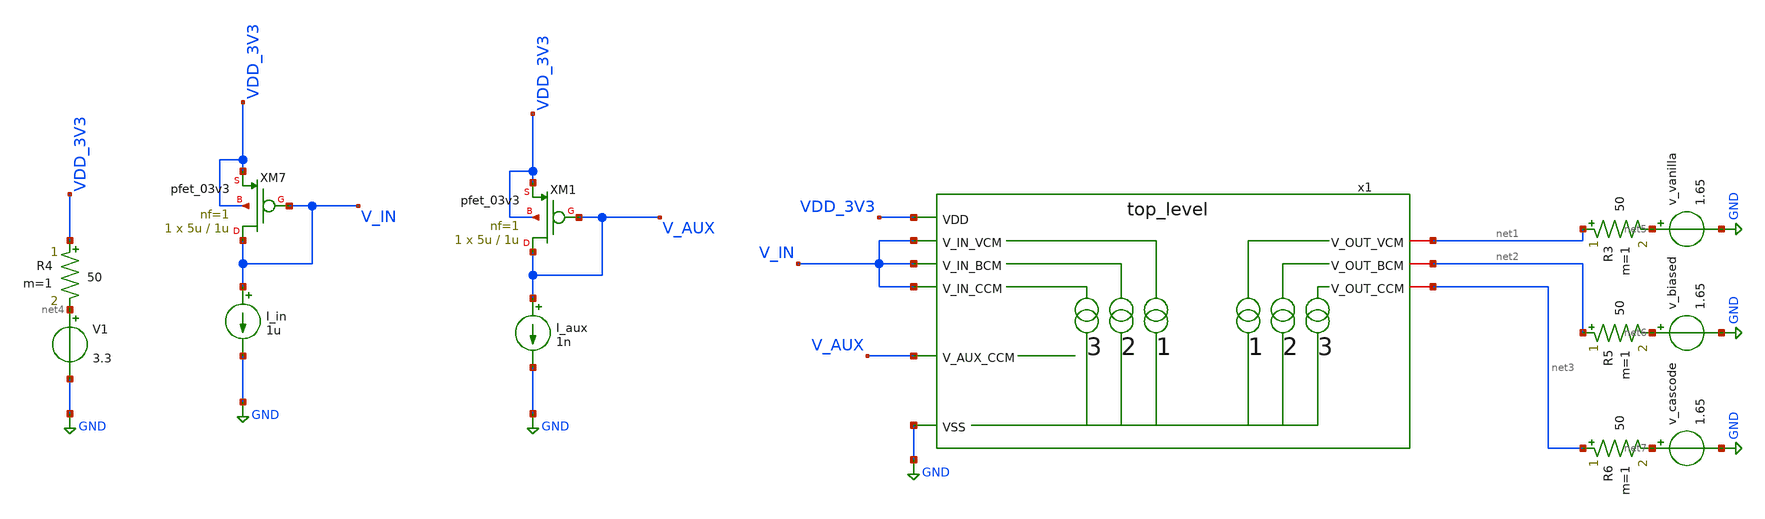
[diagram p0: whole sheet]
** sch_path: blocks/composite/regulated_cascoded_cmirror/xschem/testbench.sch
**.subckt testbench
V1 net4 GND 3.3
XM7 V_IN V_IN VDD_3V3 VDD_3V3 pfet_03v3 L=1u W=5u nf=1 ad='int((nf+1)/2) * W/nf * 0.18u' as='int((nf+2)/2) * W/nf * 0.18u'
+ pd='2*int((nf+1)/2) * (W/nf + 0.18u)' ps='2*int((nf+2)/2) * (W/nf + 0.18u)' nrd='0.18u / W' nrs='0.18u / W'
+ sa=0 sb=0 sd=0 m=1
I_in V_IN GND 1u
v_vanilla net5 GND 1.65
.save i(v_vanilla)
v_biased net6 GND 1.65
.save i(v_biased)
v_cascode net7 GND 1.65
.save i(v_cascode)
XM1 V_AUX V_AUX VDD_3V3 VDD_3V3 pfet_03v3 L=1u W=5u nf=1 ad='int((nf+1)/2) * W/nf * 0.18u' as='int((nf+2)/2) * W/nf * 0.18u'
+ pd='2*int((nf+1)/2) * (W/nf + 0.18u)' ps='2*int((nf+2)/2) * (W/nf + 0.18u)' nrd='0.18u / W' nrs='0.18u / W'
+ sa=0 sb=0 sd=0 m=1
I_aux V_AUX GND 1n
R4 VDD_3V3 net4 50 m=1
R3 net1 net5 50 m=1
R5 net2 net6 50 m=1
R6 net3 net7 50 m=1
x1 VDD_3V3 net2 V_IN net3 V_IN net1 V_IN GND V_AUX top_level
**** begin user architecture code

.include /foss/pdks/gf180mcuD/libs.tech/ngspice/design.ngspice
.lib /foss/pdks/gf180mcuD/libs.tech/ngspice/sm141064.ngspice typical




.option savecurrent

.control

save all

* --- Run vanilla sweep ---
dc v_vanilla 0 3.3 0.01
let i_vanilla = -i(v_vanilla)
wrdata vanilla.txt i_vanilla

* --- Run biased sweep ---
reset
dc v_biased 0 3.3 0.01
let i_biased = -i(v_biased)
wrdata biased.txt i_biased

* --- Run cascode sweep ---
reset
dc v_cascode 0 3.3 0.01
let i_cascode = -i(v_cascode)
wrdata cascode.txt i_cascode

.endc


**** end user architecture code
**.ends

* expanding   symbol:  top_level.sym # of pins=9
** sym_path: blocks/composite/regulated_cascoded_cmirror/xschem/top_level.sym
** sch_path: blocks/composite/regulated_cascoded_cmirror/xschem/top_level.sch
.subckt top_level VDD V_OUT_BCM V_IN_BCM V_OUT_CCM V_IN_CCM V_OUT_VCM V_IN_VCM VSS V_AUX_CCM
*.ipin VSS
*.ipin V_IN_BCM
*.ipin V_AUX_CCM
*.ipin VDD
*.iopin V_OUT_VCM
*.iopin V_OUT_BCM
*.iopin V_OUT_CCM
*.ipin V_IN_CCM
*.ipin V_IN_VCM
x1 VDD V_IN_VCM V_OUT_VCM VSS vanilla_cm
x2 VDD V_IN_BCM V_OUT_BCM VSS biased_cm
x3 VDD V_IN_CCM V_OUT_CCM VSS V_AUX_CCM cascode_cm
.ends


* expanding   symbol:  vanilla_cm.sym # of pins=4
** sym_path: blocks/composite/regulated_cascoded_cmirror/xschem/vanilla_cm.sym
** sch_path: blocks/composite/regulated_cascoded_cmirror/xschem/vanilla_cm.sch
.subckt vanilla_cm vdd v_in v_out vss
*.ipin v_in
*.ipin vdd
*.ipin vss
*.iopin v_out
XM1 v_out net1 vss vss nfet_03v3 L=1u W=5u nf=1 ad='int((nf+1)/2) * W/nf * 0.18u' as='int((nf+2)/2) * W/nf * 0.18u'
+ pd='2*int((nf+1)/2) * (W/nf + 0.18u)' ps='2*int((nf+2)/2) * (W/nf + 0.18u)' nrd='0.18u / W' nrs='0.18u / W'
+ sa=0 sb=0 sd=0 m=1
XM2 net1 net1 vss vss nfet_03v3 L=1u W=5u nf=1 ad='int((nf+1)/2) * W/nf * 0.18u' as='int((nf+2)/2) * W/nf * 0.18u'
+ pd='2*int((nf+1)/2) * (W/nf + 0.18u)' ps='2*int((nf+2)/2) * (W/nf + 0.18u)' nrd='0.18u / W' nrs='0.18u / W'
+ sa=0 sb=0 sd=0 m=1
XM9 net1 v_in vdd vdd pfet_03v3 L=1u W=5u nf=1 ad='int((nf+1)/2) * W/nf * 0.18u' as='int((nf+2)/2) * W/nf * 0.18u'
+ pd='2*int((nf+1)/2) * (W/nf + 0.18u)' ps='2*int((nf+2)/2) * (W/nf + 0.18u)' nrd='0.18u / W' nrs='0.18u / W'
+ sa=0 sb=0 sd=0 m=1
.ends


* expanding   symbol:  biased_cm.sym # of pins=4
** sym_path: blocks/composite/regulated_cascoded_cmirror/xschem/biased_cm.sym
** sch_path: blocks/composite/regulated_cascoded_cmirror/xschem/biased_cm.sch
.subckt biased_cm vdd v_in v_out vss
*.ipin v_in
*.ipin vdd
*.ipin vss
*.iopin v_out
XM3 net2 net1 vss vss nfet_03v3 L=1u W=5u nf=1 ad='int((nf+1)/2) * W/nf * 0.18u' as='int((nf+2)/2) * W/nf * 0.18u'
+ pd='2*int((nf+1)/2) * (W/nf + 0.18u)' ps='2*int((nf+2)/2) * (W/nf + 0.18u)' nrd='0.18u / W' nrs='0.18u / W'
+ sa=0 sb=0 sd=0 m=1
XM4 net1 net1 vss vss nfet_03v3 L=1u W=5u nf=1 ad='int((nf+1)/2) * W/nf * 0.18u' as='int((nf+2)/2) * W/nf * 0.18u'
+ pd='2*int((nf+1)/2) * (W/nf + 0.18u)' ps='2*int((nf+2)/2) * (W/nf + 0.18u)' nrd='0.18u / W' nrs='0.18u / W'
+ sa=0 sb=0 sd=0 m=1
XM5 v_out net3 net2 vss nfet_03v3 L=1u W=5u nf=1 ad='int((nf+1)/2) * W/nf * 0.18u' as='int((nf+2)/2) * W/nf * 0.18u'
+ pd='2*int((nf+1)/2) * (W/nf + 0.18u)' ps='2*int((nf+2)/2) * (W/nf + 0.18u)' nrd='0.18u / W' nrs='0.18u / W'
+ sa=0 sb=0 sd=0 m=1
XM6 net3 net3 net1 vss nfet_03v3 L=1u W=5u nf=1 ad='int((nf+1)/2) * W/nf * 0.18u' as='int((nf+2)/2) * W/nf * 0.18u'
+ pd='2*int((nf+1)/2) * (W/nf + 0.18u)' ps='2*int((nf+2)/2) * (W/nf + 0.18u)' nrd='0.18u / W' nrs='0.18u / W'
+ sa=0 sb=0 sd=0 m=1
XM15 net3 v_in vdd vdd pfet_03v3 L=1u W=5u nf=1 ad='int((nf+1)/2) * W/nf * 0.18u' as='int((nf+2)/2) * W/nf * 0.18u'
+ pd='2*int((nf+1)/2) * (W/nf + 0.18u)' ps='2*int((nf+2)/2) * (W/nf + 0.18u)' nrd='0.18u / W' nrs='0.18u / W'
+ sa=0 sb=0 sd=0 m=1
.ends


* expanding   symbol:  cascode_cm.sym # of pins=5
** sym_path: blocks/composite/regulated_cascoded_cmirror/xschem/cascode_cm.sym
** sch_path: blocks/composite/regulated_cascoded_cmirror/xschem/cascode_cm.sch
.subckt cascode_cm vdd v_in v_out vss v_aux
*.ipin v_in
*.ipin vdd
*.ipin vss
*.ipin v_aux
*.iopin v_out
XM10 net2 net1 vss vss nfet_03v3 L=1u W=5u nf=1 ad='int((nf+1)/2) * W/nf * 0.18u' as='int((nf+2)/2) * W/nf * 0.18u'
+ pd='2*int((nf+1)/2) * (W/nf + 0.18u)' ps='2*int((nf+2)/2) * (W/nf + 0.18u)' nrd='0.18u / W' nrs='0.18u / W'
+ sa=0 sb=0 sd=0 m=1
XM8 net4 net2 net1 vss nfet_03v3 L=1u W=5u nf=1 ad='int((nf+1)/2) * W/nf * 0.18u' as='int((nf+2)/2) * W/nf * 0.18u'
+ pd='2*int((nf+1)/2) * (W/nf + 0.18u)' ps='2*int((nf+2)/2) * (W/nf + 0.18u)' nrd='0.18u / W' nrs='0.18u / W'
+ sa=0 sb=0 sd=0 m=1
XM11 net1 net4 vss vss nfet_03v3 L=1u W=5u nf=1 ad='int((nf+1)/2) * W/nf * 0.18u' as='int((nf+2)/2) * W/nf * 0.18u'
+ pd='2*int((nf+1)/2) * (W/nf + 0.18u)' ps='2*int((nf+2)/2) * (W/nf + 0.18u)' nrd='0.18u / W' nrs='0.18u / W'
+ sa=0 sb=0 sd=0 m=1
XM12 net2 net3 vss vss nfet_03v3 L=1u W=5u nf=1 ad='int((nf+1)/2) * W/nf * 0.18u' as='int((nf+2)/2) * W/nf * 0.18u'
+ pd='2*int((nf+1)/2) * (W/nf + 0.18u)' ps='2*int((nf+2)/2) * (W/nf + 0.18u)' nrd='0.18u / W' nrs='0.18u / W'
+ sa=0 sb=0 sd=0 m=1
XM13 net3 net4 vss vss nfet_03v3 L=1u W=5u nf=1 ad='int((nf+1)/2) * W/nf * 0.18u' as='int((nf+2)/2) * W/nf * 0.18u'
+ pd='2*int((nf+1)/2) * (W/nf + 0.18u)' ps='2*int((nf+2)/2) * (W/nf + 0.18u)' nrd='0.18u / W' nrs='0.18u / W'
+ sa=0 sb=0 sd=0 m=1
XM14 v_out net2 net3 vss nfet_03v3 L=1u W=5u nf=1 ad='int((nf+1)/2) * W/nf * 0.18u' as='int((nf+2)/2) * W/nf * 0.18u'
+ pd='2*int((nf+1)/2) * (W/nf + 0.18u)' ps='2*int((nf+2)/2) * (W/nf + 0.18u)' nrd='0.18u / W' nrs='0.18u / W'
+ sa=0 sb=0 sd=0 m=1
XM16 net4 v_in vdd vdd pfet_03v3 L=1u W=5u nf=1 ad='int((nf+1)/2) * W/nf * 0.18u' as='int((nf+2)/2) * W/nf * 0.18u'
+ pd='2*int((nf+1)/2) * (W/nf + 0.18u)' ps='2*int((nf+2)/2) * (W/nf + 0.18u)' nrd='0.18u / W' nrs='0.18u / W'
+ sa=0 sb=0 sd=0 m=1
XM18 net2 v_aux vdd vdd pfet_03v3 L=1u W=5u nf=1 ad='int((nf+1)/2) * W/nf * 0.18u' as='int((nf+2)/2) * W/nf * 0.18u'
+ pd='2*int((nf+1)/2) * (W/nf + 0.18u)' ps='2*int((nf+2)/2) * (W/nf + 0.18u)' nrd='0.18u / W' nrs='0.18u / W'
+ sa=0 sb=0 sd=0 m=1
.ends

.GLOBAL GND
.end
